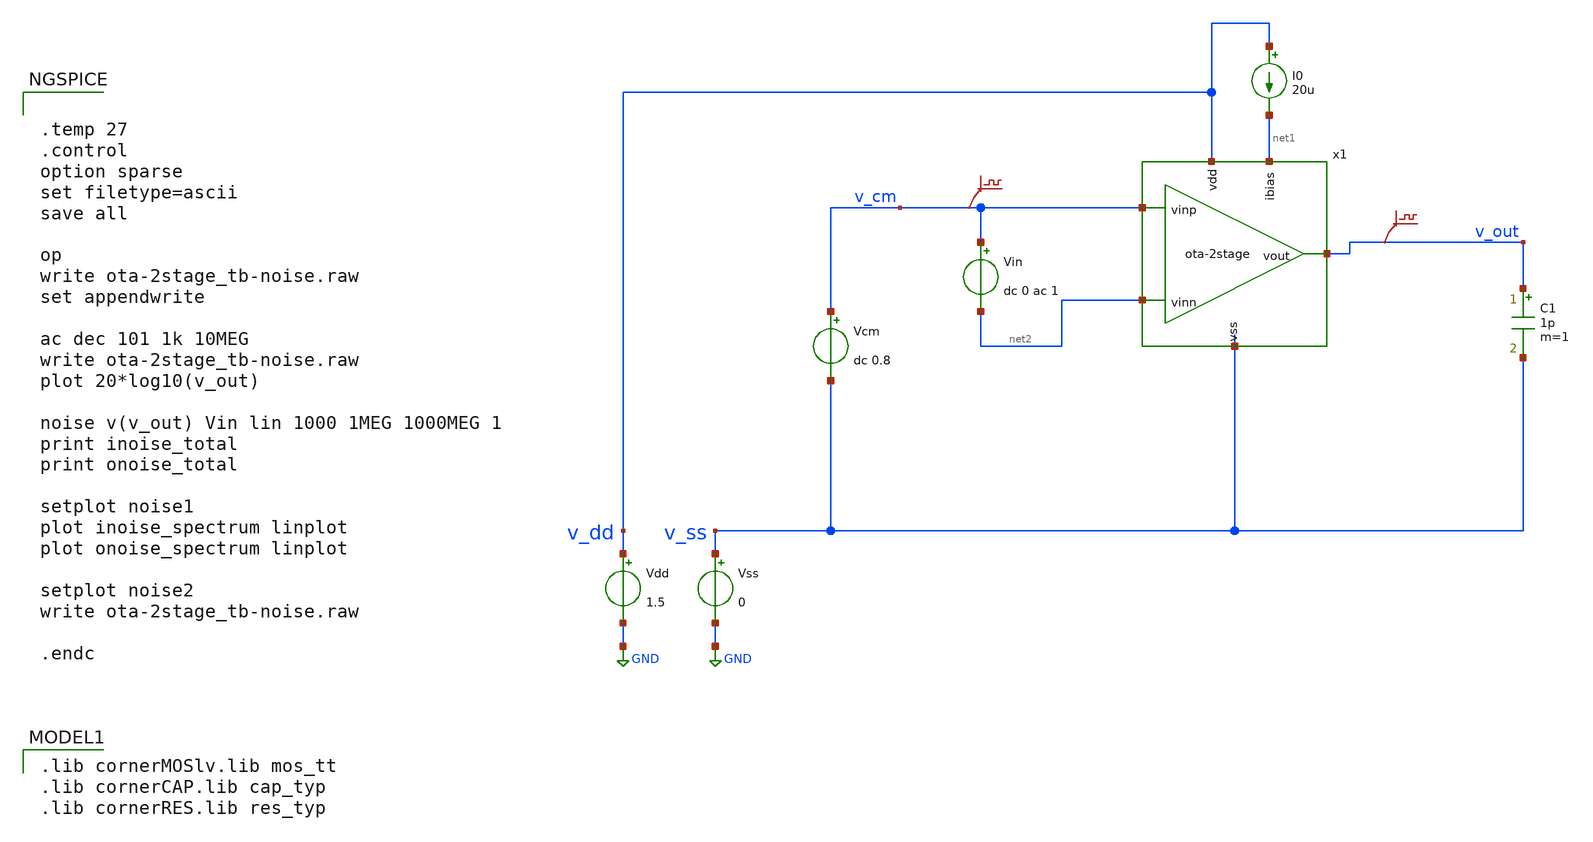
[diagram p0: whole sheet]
** sch_path: xschem/ota-2stage_tb-noise.sch
**.subckt ota-2stage_tb-noise
Vdd v_dd GND 1.5
Vss v_ss GND 0
C1 v_out v_ss 1p m=1
Vcm v_cm v_ss dc 0.8
I0 v_dd net1 20u
.save v(v_cm)
.save v(v_out)
Vin v_cm net2 dc 0 ac 1
x1 v_dd net1 net2 v_out v_cm v_ss ota-2stage
**** begin user architecture code


.temp 27
.control
option sparse
set filetype=ascii
save all

op
write ota-2stage_tb-noise.raw
set appendwrite

ac dec 101 1k 10MEG
write ota-2stage_tb-noise.raw
plot 20*log10(v_out)

noise v(v_out) Vin lin 1000 1MEG 1000MEG 1
print inoise_total
print onoise_total

setplot noise1
plot inoise_spectrum linplot
plot onoise_spectrum linplot

setplot noise2
write ota-2stage_tb-noise.raw

.endc


 .lib cornerMOSlv.lib mos_tt
.lib cornerCAP.lib cap_typ
.lib cornerRES.lib res_typ

**** end user architecture code
**.ends
.GLOBAL GND
.end
